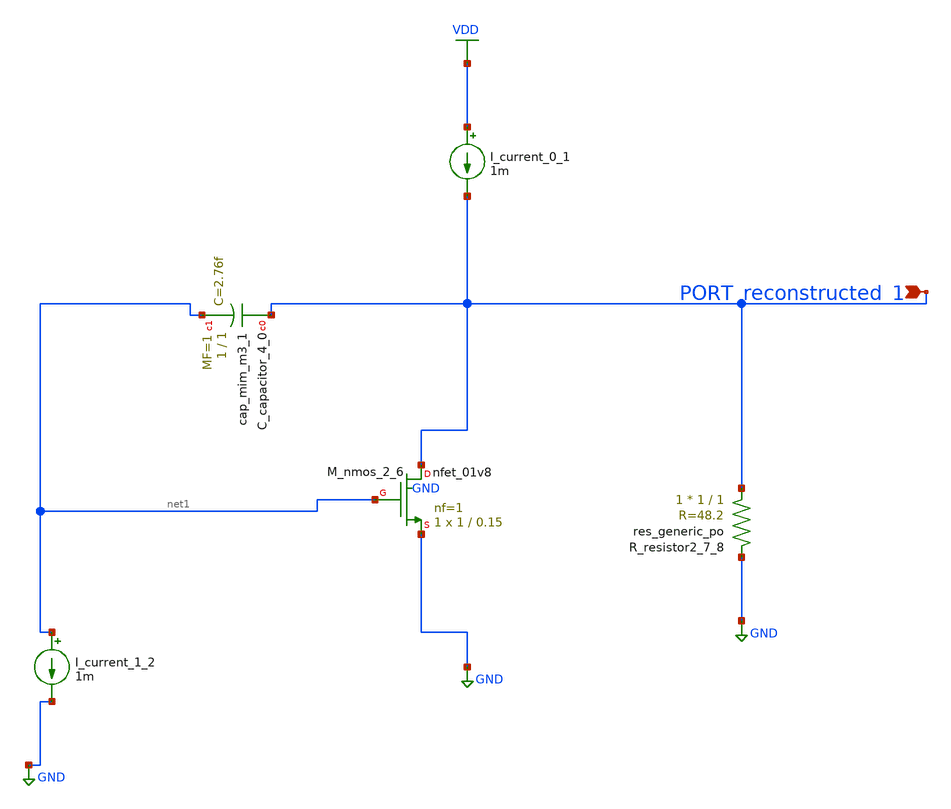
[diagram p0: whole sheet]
** sch_path: schematics/AMSNet/728.sch
**.subckt 728 PORT_reconstructed_1
*.ipin PORT_reconstructed_1
XC_capacitor_4_0 PORT_reconstructed_1 net1 sky130_fd_pr__cap_mim_m3_1 W=1 L=1 MF=1 m=1
I_current_0_1 VDD PORT_reconstructed_1 1m
I_current_1_2 net1 GND 1m
XM_nmos_2_6 PORT_reconstructed_1 net1 GND GND sky130_fd_pr__nfet_01v8 L=0.15 W=1 nf=1 ad='int((1 + 1)/2) * 1 / 1 * 0.29'
+ as='int((1 + 2)/2) * 1 / 1 * 0.29' pd='2*int((1 + 1)/2) * (1 / 1 + 0.29)' ps='2*int((1 + 2)/2) * (1 / 1 + 0.29)'
+ nrd='0.29 / 1 ' nrs='0.29 / 1 ' sa=0 sb=0 sd=0 mult=1 m=1
XR_resistor2_7_8 PORT_reconstructed_1 GND sky130_fd_pr__res_generic_po W=1 L=1 m=1
**.ends
.GLOBAL GND
.GLOBAL VDD
.end
